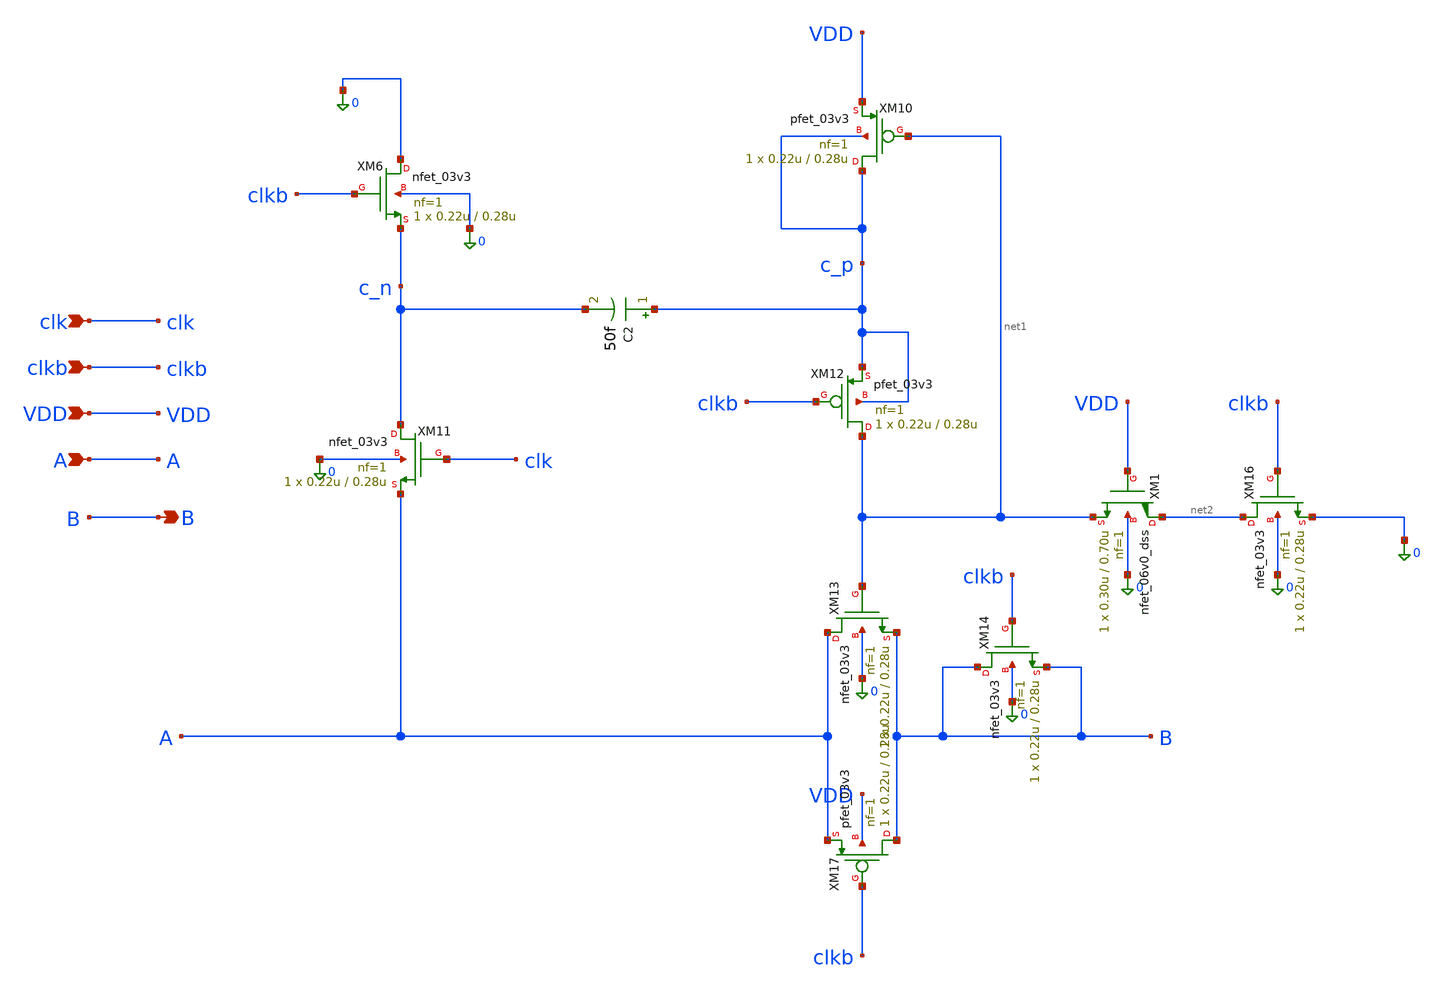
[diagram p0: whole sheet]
** sch_path: Design_Files/IC Design/Schematic/SAR_ADC_BLOCKS/BSW/BSW.sch
**.subckt BSW clk clkb VDD A B
*.ipin clk
*.ipin clkb
*.ipin VDD
*.ipin A
*.opin B
C2 c_p c_n 50f m=1
XM6 0 clkb c_n 0 nfet_03v3 L=0.28u W=0.22u nf=1 ad='int((nf+1)/2) * W/nf * 0.18u' as='int((nf+2)/2) * W/nf * 0.18u'
+ pd='2*int((nf+1)/2) * (W/nf + 0.18u)' ps='2*int((nf+2)/2) * (W/nf + 0.18u)' nrd='0.18u / W' nrs='0.18u / W'
+ sa=0 sb=0 sd=0 m=1
XM10 c_p net1 VDD c_p pfet_03v3 L=0.28u W=0.22u nf=1 ad='int((nf+1)/2) * W/nf * 0.18u' as='int((nf+2)/2) * W/nf * 0.18u'
+ pd='2*int((nf+1)/2) * (W/nf + 0.18u)' ps='2*int((nf+2)/2) * (W/nf + 0.18u)' nrd='0.18u / W' nrs='0.18u / W'
+ sa=0 sb=0 sd=0 m=1
XM11 c_n clk A 0 nfet_03v3 L=0.28u W=0.22u nf=1 ad='int((nf+1)/2) * W/nf * 0.18u' as='int((nf+2)/2) * W/nf * 0.18u'
+ pd='2*int((nf+1)/2) * (W/nf + 0.18u)' ps='2*int((nf+2)/2) * (W/nf + 0.18u)' nrd='0.18u / W' nrs='0.18u / W'
+ sa=0 sb=0 sd=0 m=1
XM12 net1 clkb c_p c_p pfet_03v3 L=0.28u W=0.22u nf=1 ad='int((nf+1)/2) * W/nf * 0.18u' as='int((nf+2)/2) * W/nf * 0.18u'
+ pd='2*int((nf+1)/2) * (W/nf + 0.18u)' ps='2*int((nf+2)/2) * (W/nf + 0.18u)' nrd='0.18u / W' nrs='0.18u / W'
+ sa=0 sb=0 sd=0 m=1
XM13 A net1 B 0 nfet_03v3 L=0.28u W=0.22u nf=1 ad='int((nf+1)/2) * W/nf * 0.18u' as='int((nf+2)/2) * W/nf * 0.18u'
+ pd='2*int((nf+1)/2) * (W/nf + 0.18u)' ps='2*int((nf+2)/2) * (W/nf + 0.18u)' nrd='0.18u / W' nrs='0.18u / W'
+ sa=0 sb=0 sd=0 m=1
XM14 B clkb B 0 nfet_03v3 L=0.28u W=0.22u nf=1 ad='int((nf+1)/2) * W/nf * 0.18u' as='int((nf+2)/2) * W/nf * 0.18u'
+ pd='2*int((nf+1)/2) * (W/nf + 0.18u)' ps='2*int((nf+2)/2) * (W/nf + 0.18u)' nrd='0.18u / W' nrs='0.18u / W'
+ sa=0 sb=0 sd=0 m=1
XM16 net2 clkb 0 0 nfet_03v3 L=0.28u W=0.22u nf=1 ad='int((nf+1)/2) * W/nf * 0.18u' as='int((nf+2)/2) * W/nf * 0.18u'
+ pd='2*int((nf+1)/2) * (W/nf + 0.18u)' ps='2*int((nf+2)/2) * (W/nf + 0.18u)' nrd='0.18u / W' nrs='0.18u / W'
+ sa=0 sb=0 sd=0 m=1
XM17 B clkb A VDD pfet_03v3 L=0.28u W=0.22u nf=1 ad='int((nf+1)/2) * W/nf * 0.18u' as='int((nf+2)/2) * W/nf * 0.18u'
+ pd='2*int((nf+1)/2) * (W/nf + 0.18u)' ps='2*int((nf+2)/2) * (W/nf + 0.18u)' nrd='0.18u / W' nrs='0.18u / W'
+ sa=0 sb=0 sd=0 m=1
XM1 net2 VDD net1 0 nfet_06v0_dss L=0.70u W=0.30u nf=1 ad='int((nf+1)/2) * W/nf * 0.18u' as='int((nf+2)/2) * W/nf * 0.18u'
+ pd='2*int((nf+1)/2) * (W/nf + 0.18u)' ps='2*int((nf+2)/2) * (W/nf + 0.18u)' nrd='0.18u / W' nrs='0.18u / W'
+ sa=0 sb=0 sd=0 m=1
**.ends
.end
